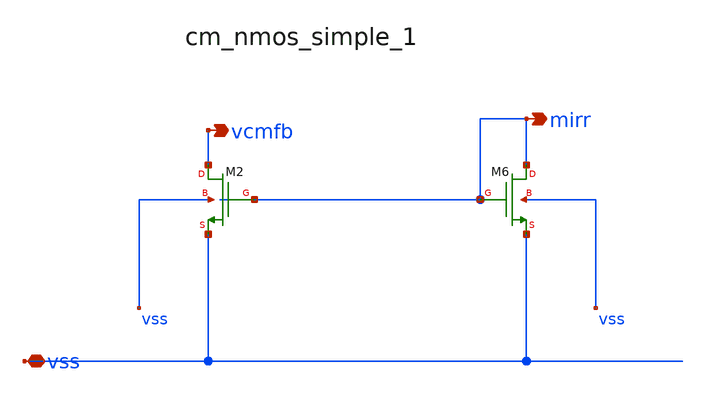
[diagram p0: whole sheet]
** sch_path: analog-db/raw/cmfb_002_5t_pmos_input/hier/blocks/cm_nmos_simple_1.sch
**.subckt cm_nmos_simple_1 vss vcmfb mirr
*.iopin vss
*.opin vcmfb
*.opin mirr
XM2 vcmfb mirr vss vss sg13_lv_nmos w=x_dut_xm2_w l=x_dut_xm2_l ng=1 m=x_dut_xm2_m
XM6 mirr mirr vss vss sg13_lv_nmos w=x_dut_xm6_w l=x_dut_xm6_l ng=1 m=x_dut_xm6_m
**.ends
.end
